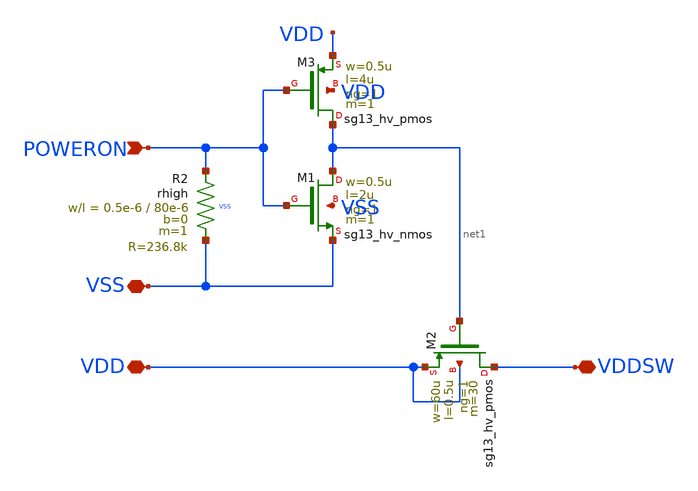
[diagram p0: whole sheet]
** sch_path: ip/util/xschem/powersw.sch
**.subckt powersw VDD POWERON VDDSW VSS
*.iopin VDD
*.ipin POWERON
*.iopin VDDSW
*.iopin VSS
XM2 VDDSW net1 VDD VDD sg13_hv_pmos w=60u l=0.5u ng=1 m=30 mm_ok=1
XM1 net1 POWERON VSS VSS sg13_hv_nmos w=0.5u l=2u ng=1 m=1 mm_ok=1
XR2 POWERON VSS VSS rhigh w=0.5e-6 l=80e-6 m=1 b=0 mm_ok=1
XM3 net1 POWERON VDD VDD sg13_hv_pmos w=0.5u l=4u ng=1 m=1 mm_ok=1
**.ends
.end
